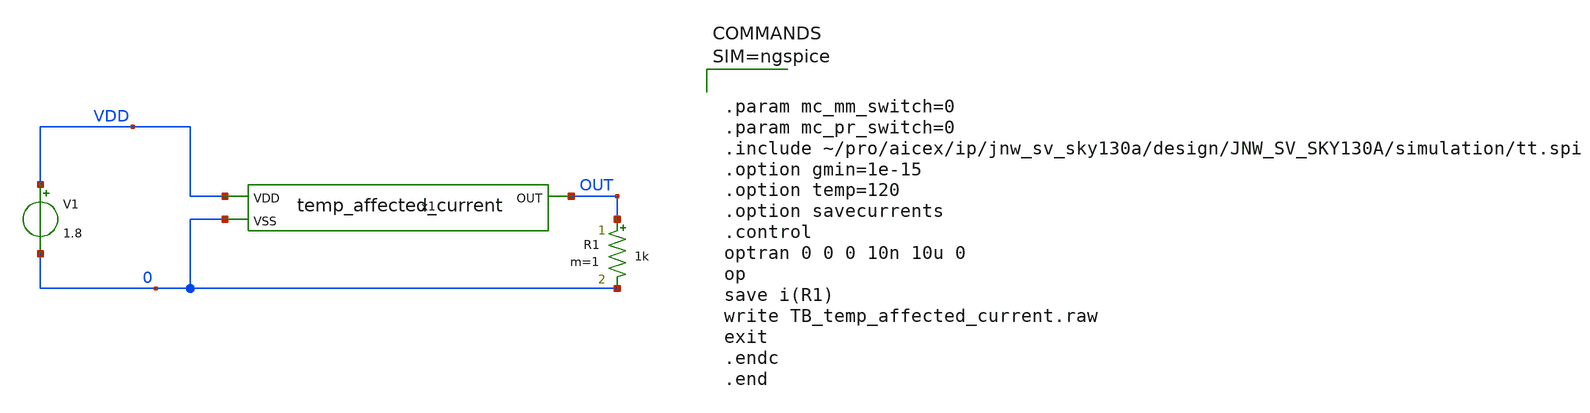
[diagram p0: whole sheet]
** sch_path: design/JNW_GR06_SKY130A/TB_temp_affected_current.sch
**.subckt TB_temp_affected_current
x1 VDD OUT 0 temp_affected_current
R1 OUT 0 1k m=1
V1 VDD 0 1.8
**** begin user architecture code



.param mc_mm_switch=0
.param mc_pr_switch=0
.include ~/pro/aicex/ip/jnw_sv_sky130a/design/JNW_SV_SKY130A/simulation/tt.spi
.option gmin=1e-15
.option temp=120
.option savecurrents
.control
optran 0 0 0 10n 10u 0
op
save i(R1)
write TB_temp_affected_current.raw
exit
.endc
.end



**** end user architecture code
**.ends
.end
